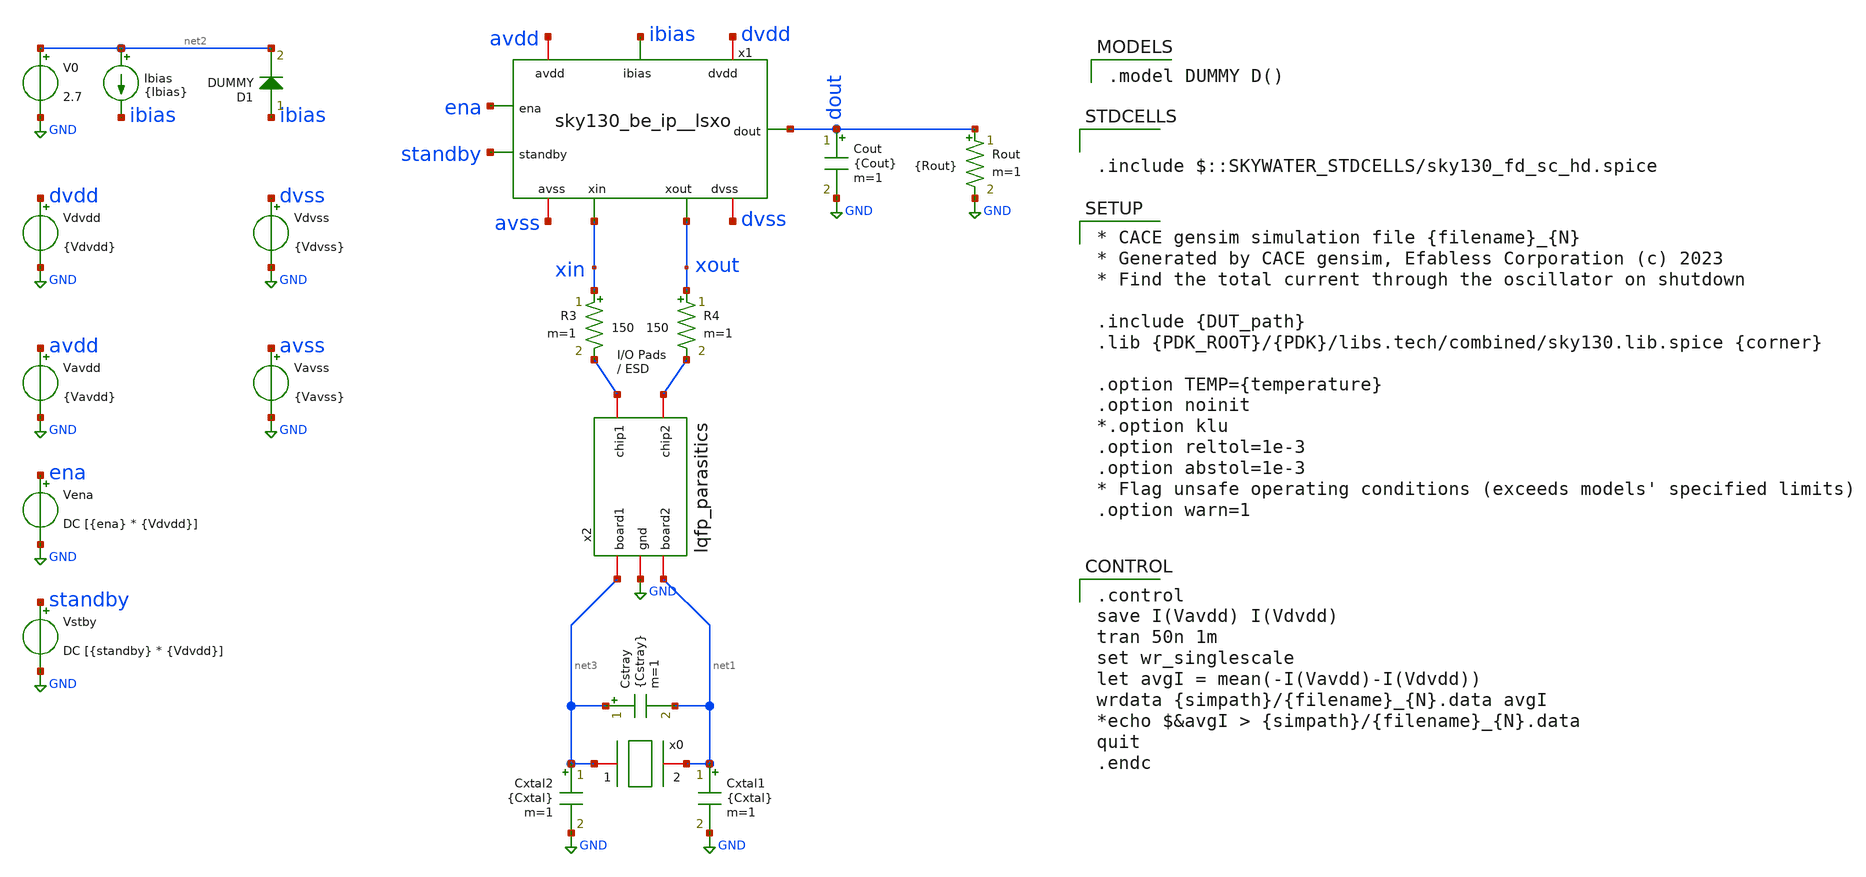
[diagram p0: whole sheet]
** sch_path: cace/tb_current_total.sch

.include $::SKYWATER_STDCELLS/sky130_fd_sc_hd.spice

**.subckt tb_current_total
Vdvdd dvdd GND {Vdvdd}
Vavdd avdd GND {Vavdd}
Cxtal2 net3 GND {Cxtal} m=1
Cxtal1 net1 GND {Cxtal} m=1
Cstray net3 net1 {Cstray} m=1
Ibias net2 ibias {Ibias}
Cout dout GND {Cout} m=1
V0 net2 GND 2.7
Vstby standby GND DC [{standby} * {Vdvdd}]
R3 xin net4 150 m=1
R4 xout net5 150 m=1
x2 net5 net4 GND net3 net1 lqfp_parasitics
Vena ena GND DC [{ena} * {Vdvdd}]
D1 ibias net2 DUMMY area=100
x1 avdd avss dvdd dvss ibias ena standby dout xin xout sky130_be_ip__lsxo
Vdvss dvss GND {Vdvss}
Vavss avss GND {Vavss}
Rout dout GND {Rout} m=1
x0 net3 net1 xtal_iqd_125_1
**** begin user architecture code

.model DUMMY D()


.control
save I(Vavdd) I(Vdvdd)
tran 50n 1m
set wr_singlescale
let avgI = mean(-I(Vavdd)-I(Vdvdd))
wrdata {simpath}/{filename}_{N}.data avgI
*echo $&avgI > {simpath}/{filename}_{N}.data
quit
.endc



* CACE gensim simulation file {filename}_{N}
* Generated by CACE gensim, Efabless Corporation (c) 2023
* Find the total current through the oscillator on shutdown

.include {DUT_path}
.lib {PDK_ROOT}/{PDK}/libs.tech/combined/sky130.lib.spice {corner}

.option TEMP={temperature}
.option noinit
*.option klu
.option reltol=1e-3
.option abstol=1e-3
* Flag unsafe operating conditions (exceeds models' specified limits)
.option warn=1


**** end user architecture code
**.ends
.GLOBAL GND
.end
